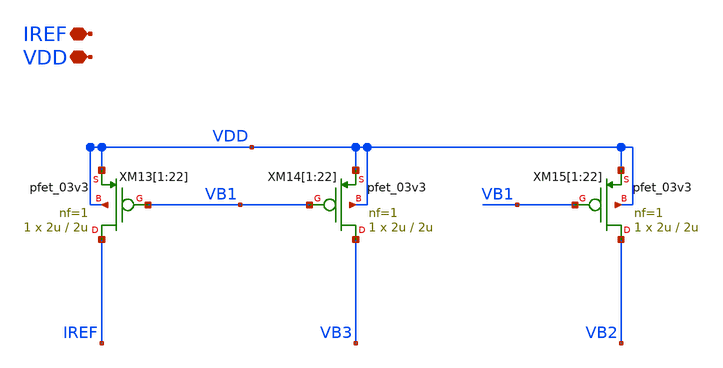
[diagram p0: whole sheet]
** sch_path: TIA_Filter/Folded/FC_bias_pfets.sch
**.subckt FC_bias_pfets IREF VDD
*.iopin IREF
*.iopin VDD
XM13[1] IREF VB1 VDD VDD pfet_03v3 L=2u W=2u nf=1 ad='int((nf+1)/2) * W/nf * 0.18u' as='int((nf+2)/2) * W/nf * 0.18u'
+ pd='2*int((nf+1)/2) * (W/nf + 0.18u)' ps='2*int((nf+2)/2) * (W/nf + 0.18u)' nrd='0.18u / W' nrs='0.18u / W'
+ sa=0 sb=0 sd=0 m=1
XM13[2] IREF VB1 VDD VDD pfet_03v3 L=2u W=2u nf=1 ad='int((nf+1)/2) * W/nf * 0.18u' as='int((nf+2)/2) * W/nf * 0.18u'
+ pd='2*int((nf+1)/2) * (W/nf + 0.18u)' ps='2*int((nf+2)/2) * (W/nf + 0.18u)' nrd='0.18u / W' nrs='0.18u / W'
+ sa=0 sb=0 sd=0 m=1
XM13[3] IREF VB1 VDD VDD pfet_03v3 L=2u W=2u nf=1 ad='int((nf+1)/2) * W/nf * 0.18u' as='int((nf+2)/2) * W/nf * 0.18u'
+ pd='2*int((nf+1)/2) * (W/nf + 0.18u)' ps='2*int((nf+2)/2) * (W/nf + 0.18u)' nrd='0.18u / W' nrs='0.18u / W'
+ sa=0 sb=0 sd=0 m=1
XM13[4] IREF VB1 VDD VDD pfet_03v3 L=2u W=2u nf=1 ad='int((nf+1)/2) * W/nf * 0.18u' as='int((nf+2)/2) * W/nf * 0.18u'
+ pd='2*int((nf+1)/2) * (W/nf + 0.18u)' ps='2*int((nf+2)/2) * (W/nf + 0.18u)' nrd='0.18u / W' nrs='0.18u / W'
+ sa=0 sb=0 sd=0 m=1
XM13[5] IREF VB1 VDD VDD pfet_03v3 L=2u W=2u nf=1 ad='int((nf+1)/2) * W/nf * 0.18u' as='int((nf+2)/2) * W/nf * 0.18u'
+ pd='2*int((nf+1)/2) * (W/nf + 0.18u)' ps='2*int((nf+2)/2) * (W/nf + 0.18u)' nrd='0.18u / W' nrs='0.18u / W'
+ sa=0 sb=0 sd=0 m=1
XM13[6] IREF VB1 VDD VDD pfet_03v3 L=2u W=2u nf=1 ad='int((nf+1)/2) * W/nf * 0.18u' as='int((nf+2)/2) * W/nf * 0.18u'
+ pd='2*int((nf+1)/2) * (W/nf + 0.18u)' ps='2*int((nf+2)/2) * (W/nf + 0.18u)' nrd='0.18u / W' nrs='0.18u / W'
+ sa=0 sb=0 sd=0 m=1
XM13[7] IREF VB1 VDD VDD pfet_03v3 L=2u W=2u nf=1 ad='int((nf+1)/2) * W/nf * 0.18u' as='int((nf+2)/2) * W/nf * 0.18u'
+ pd='2*int((nf+1)/2) * (W/nf + 0.18u)' ps='2*int((nf+2)/2) * (W/nf + 0.18u)' nrd='0.18u / W' nrs='0.18u / W'
+ sa=0 sb=0 sd=0 m=1
XM13[8] IREF VB1 VDD VDD pfet_03v3 L=2u W=2u nf=1 ad='int((nf+1)/2) * W/nf * 0.18u' as='int((nf+2)/2) * W/nf * 0.18u'
+ pd='2*int((nf+1)/2) * (W/nf + 0.18u)' ps='2*int((nf+2)/2) * (W/nf + 0.18u)' nrd='0.18u / W' nrs='0.18u / W'
+ sa=0 sb=0 sd=0 m=1
XM13[9] IREF VB1 VDD VDD pfet_03v3 L=2u W=2u nf=1 ad='int((nf+1)/2) * W/nf * 0.18u' as='int((nf+2)/2) * W/nf * 0.18u'
+ pd='2*int((nf+1)/2) * (W/nf + 0.18u)' ps='2*int((nf+2)/2) * (W/nf + 0.18u)' nrd='0.18u / W' nrs='0.18u / W'
+ sa=0 sb=0 sd=0 m=1
XM13[10] IREF VB1 VDD VDD pfet_03v3 L=2u W=2u nf=1 ad='int((nf+1)/2) * W/nf * 0.18u' as='int((nf+2)/2) * W/nf * 0.18u'
+ pd='2*int((nf+1)/2) * (W/nf + 0.18u)' ps='2*int((nf+2)/2) * (W/nf + 0.18u)' nrd='0.18u / W' nrs='0.18u / W'
+ sa=0 sb=0 sd=0 m=1
XM13[11] IREF VB1 VDD VDD pfet_03v3 L=2u W=2u nf=1 ad='int((nf+1)/2) * W/nf * 0.18u' as='int((nf+2)/2) * W/nf * 0.18u'
+ pd='2*int((nf+1)/2) * (W/nf + 0.18u)' ps='2*int((nf+2)/2) * (W/nf + 0.18u)' nrd='0.18u / W' nrs='0.18u / W'
+ sa=0 sb=0 sd=0 m=1
XM13[12] IREF VB1 VDD VDD pfet_03v3 L=2u W=2u nf=1 ad='int((nf+1)/2) * W/nf * 0.18u' as='int((nf+2)/2) * W/nf * 0.18u'
+ pd='2*int((nf+1)/2) * (W/nf + 0.18u)' ps='2*int((nf+2)/2) * (W/nf + 0.18u)' nrd='0.18u / W' nrs='0.18u / W'
+ sa=0 sb=0 sd=0 m=1
XM13[13] IREF VB1 VDD VDD pfet_03v3 L=2u W=2u nf=1 ad='int((nf+1)/2) * W/nf * 0.18u' as='int((nf+2)/2) * W/nf * 0.18u'
+ pd='2*int((nf+1)/2) * (W/nf + 0.18u)' ps='2*int((nf+2)/2) * (W/nf + 0.18u)' nrd='0.18u / W' nrs='0.18u / W'
+ sa=0 sb=0 sd=0 m=1
XM13[14] IREF VB1 VDD VDD pfet_03v3 L=2u W=2u nf=1 ad='int((nf+1)/2) * W/nf * 0.18u' as='int((nf+2)/2) * W/nf * 0.18u'
+ pd='2*int((nf+1)/2) * (W/nf + 0.18u)' ps='2*int((nf+2)/2) * (W/nf + 0.18u)' nrd='0.18u / W' nrs='0.18u / W'
+ sa=0 sb=0 sd=0 m=1
XM13[15] IREF VB1 VDD VDD pfet_03v3 L=2u W=2u nf=1 ad='int((nf+1)/2) * W/nf * 0.18u' as='int((nf+2)/2) * W/nf * 0.18u'
+ pd='2*int((nf+1)/2) * (W/nf + 0.18u)' ps='2*int((nf+2)/2) * (W/nf + 0.18u)' nrd='0.18u / W' nrs='0.18u / W'
+ sa=0 sb=0 sd=0 m=1
XM13[16] IREF VB1 VDD VDD pfet_03v3 L=2u W=2u nf=1 ad='int((nf+1)/2) * W/nf * 0.18u' as='int((nf+2)/2) * W/nf * 0.18u'
+ pd='2*int((nf+1)/2) * (W/nf + 0.18u)' ps='2*int((nf+2)/2) * (W/nf + 0.18u)' nrd='0.18u / W' nrs='0.18u / W'
+ sa=0 sb=0 sd=0 m=1
XM13[17] IREF VB1 VDD VDD pfet_03v3 L=2u W=2u nf=1 ad='int((nf+1)/2) * W/nf * 0.18u' as='int((nf+2)/2) * W/nf * 0.18u'
+ pd='2*int((nf+1)/2) * (W/nf + 0.18u)' ps='2*int((nf+2)/2) * (W/nf + 0.18u)' nrd='0.18u / W' nrs='0.18u / W'
+ sa=0 sb=0 sd=0 m=1
XM13[18] IREF VB1 VDD VDD pfet_03v3 L=2u W=2u nf=1 ad='int((nf+1)/2) * W/nf * 0.18u' as='int((nf+2)/2) * W/nf * 0.18u'
+ pd='2*int((nf+1)/2) * (W/nf + 0.18u)' ps='2*int((nf+2)/2) * (W/nf + 0.18u)' nrd='0.18u / W' nrs='0.18u / W'
+ sa=0 sb=0 sd=0 m=1
XM13[19] IREF VB1 VDD VDD pfet_03v3 L=2u W=2u nf=1 ad='int((nf+1)/2) * W/nf * 0.18u' as='int((nf+2)/2) * W/nf * 0.18u'
+ pd='2*int((nf+1)/2) * (W/nf + 0.18u)' ps='2*int((nf+2)/2) * (W/nf + 0.18u)' nrd='0.18u / W' nrs='0.18u / W'
+ sa=0 sb=0 sd=0 m=1
XM13[20] IREF VB1 VDD VDD pfet_03v3 L=2u W=2u nf=1 ad='int((nf+1)/2) * W/nf * 0.18u' as='int((nf+2)/2) * W/nf * 0.18u'
+ pd='2*int((nf+1)/2) * (W/nf + 0.18u)' ps='2*int((nf+2)/2) * (W/nf + 0.18u)' nrd='0.18u / W' nrs='0.18u / W'
+ sa=0 sb=0 sd=0 m=1
XM13[21] IREF VB1 VDD VDD pfet_03v3 L=2u W=2u nf=1 ad='int((nf+1)/2) * W/nf * 0.18u' as='int((nf+2)/2) * W/nf * 0.18u'
+ pd='2*int((nf+1)/2) * (W/nf + 0.18u)' ps='2*int((nf+2)/2) * (W/nf + 0.18u)' nrd='0.18u / W' nrs='0.18u / W'
+ sa=0 sb=0 sd=0 m=1
XM13[22] IREF VB1 VDD VDD pfet_03v3 L=2u W=2u nf=1 ad='int((nf+1)/2) * W/nf * 0.18u' as='int((nf+2)/2) * W/nf * 0.18u'
+ pd='2*int((nf+1)/2) * (W/nf + 0.18u)' ps='2*int((nf+2)/2) * (W/nf + 0.18u)' nrd='0.18u / W' nrs='0.18u / W'
+ sa=0 sb=0 sd=0 m=1
XM14[1] VB3 VB1 VDD VDD pfet_03v3 L=2u W=2u nf=1 ad='int((nf+1)/2) * W/nf * 0.18u' as='int((nf+2)/2) * W/nf * 0.18u'
+ pd='2*int((nf+1)/2) * (W/nf + 0.18u)' ps='2*int((nf+2)/2) * (W/nf + 0.18u)' nrd='0.18u / W' nrs='0.18u / W'
+ sa=0 sb=0 sd=0 m=1
XM14[2] VB3 VB1 VDD VDD pfet_03v3 L=2u W=2u nf=1 ad='int((nf+1)/2) * W/nf * 0.18u' as='int((nf+2)/2) * W/nf * 0.18u'
+ pd='2*int((nf+1)/2) * (W/nf + 0.18u)' ps='2*int((nf+2)/2) * (W/nf + 0.18u)' nrd='0.18u / W' nrs='0.18u / W'
+ sa=0 sb=0 sd=0 m=1
XM14[3] VB3 VB1 VDD VDD pfet_03v3 L=2u W=2u nf=1 ad='int((nf+1)/2) * W/nf * 0.18u' as='int((nf+2)/2) * W/nf * 0.18u'
+ pd='2*int((nf+1)/2) * (W/nf + 0.18u)' ps='2*int((nf+2)/2) * (W/nf + 0.18u)' nrd='0.18u / W' nrs='0.18u / W'
+ sa=0 sb=0 sd=0 m=1
XM14[4] VB3 VB1 VDD VDD pfet_03v3 L=2u W=2u nf=1 ad='int((nf+1)/2) * W/nf * 0.18u' as='int((nf+2)/2) * W/nf * 0.18u'
+ pd='2*int((nf+1)/2) * (W/nf + 0.18u)' ps='2*int((nf+2)/2) * (W/nf + 0.18u)' nrd='0.18u / W' nrs='0.18u / W'
+ sa=0 sb=0 sd=0 m=1
XM14[5] VB3 VB1 VDD VDD pfet_03v3 L=2u W=2u nf=1 ad='int((nf+1)/2) * W/nf * 0.18u' as='int((nf+2)/2) * W/nf * 0.18u'
+ pd='2*int((nf+1)/2) * (W/nf + 0.18u)' ps='2*int((nf+2)/2) * (W/nf + 0.18u)' nrd='0.18u / W' nrs='0.18u / W'
+ sa=0 sb=0 sd=0 m=1
XM14[6] VB3 VB1 VDD VDD pfet_03v3 L=2u W=2u nf=1 ad='int((nf+1)/2) * W/nf * 0.18u' as='int((nf+2)/2) * W/nf * 0.18u'
+ pd='2*int((nf+1)/2) * (W/nf + 0.18u)' ps='2*int((nf+2)/2) * (W/nf + 0.18u)' nrd='0.18u / W' nrs='0.18u / W'
+ sa=0 sb=0 sd=0 m=1
XM14[7] VB3 VB1 VDD VDD pfet_03v3 L=2u W=2u nf=1 ad='int((nf+1)/2) * W/nf * 0.18u' as='int((nf+2)/2) * W/nf * 0.18u'
+ pd='2*int((nf+1)/2) * (W/nf + 0.18u)' ps='2*int((nf+2)/2) * (W/nf + 0.18u)' nrd='0.18u / W' nrs='0.18u / W'
+ sa=0 sb=0 sd=0 m=1
XM14[8] VB3 VB1 VDD VDD pfet_03v3 L=2u W=2u nf=1 ad='int((nf+1)/2) * W/nf * 0.18u' as='int((nf+2)/2) * W/nf * 0.18u'
+ pd='2*int((nf+1)/2) * (W/nf + 0.18u)' ps='2*int((nf+2)/2) * (W/nf + 0.18u)' nrd='0.18u / W' nrs='0.18u / W'
+ sa=0 sb=0 sd=0 m=1
XM14[9] VB3 VB1 VDD VDD pfet_03v3 L=2u W=2u nf=1 ad='int((nf+1)/2) * W/nf * 0.18u' as='int((nf+2)/2) * W/nf * 0.18u'
+ pd='2*int((nf+1)/2) * (W/nf + 0.18u)' ps='2*int((nf+2)/2) * (W/nf + 0.18u)' nrd='0.18u / W' nrs='0.18u / W'
+ sa=0 sb=0 sd=0 m=1
XM14[10] VB3 VB1 VDD VDD pfet_03v3 L=2u W=2u nf=1 ad='int((nf+1)/2) * W/nf * 0.18u' as='int((nf+2)/2) * W/nf * 0.18u'
+ pd='2*int((nf+1)/2) * (W/nf + 0.18u)' ps='2*int((nf+2)/2) * (W/nf + 0.18u)' nrd='0.18u / W' nrs='0.18u / W'
+ sa=0 sb=0 sd=0 m=1
XM14[11] VB3 VB1 VDD VDD pfet_03v3 L=2u W=2u nf=1 ad='int((nf+1)/2) * W/nf * 0.18u' as='int((nf+2)/2) * W/nf * 0.18u'
+ pd='2*int((nf+1)/2) * (W/nf + 0.18u)' ps='2*int((nf+2)/2) * (W/nf + 0.18u)' nrd='0.18u / W' nrs='0.18u / W'
+ sa=0 sb=0 sd=0 m=1
XM14[12] VB3 VB1 VDD VDD pfet_03v3 L=2u W=2u nf=1 ad='int((nf+1)/2) * W/nf * 0.18u' as='int((nf+2)/2) * W/nf * 0.18u'
+ pd='2*int((nf+1)/2) * (W/nf + 0.18u)' ps='2*int((nf+2)/2) * (W/nf + 0.18u)' nrd='0.18u / W' nrs='0.18u / W'
+ sa=0 sb=0 sd=0 m=1
XM14[13] VB3 VB1 VDD VDD pfet_03v3 L=2u W=2u nf=1 ad='int((nf+1)/2) * W/nf * 0.18u' as='int((nf+2)/2) * W/nf * 0.18u'
+ pd='2*int((nf+1)/2) * (W/nf + 0.18u)' ps='2*int((nf+2)/2) * (W/nf + 0.18u)' nrd='0.18u / W' nrs='0.18u / W'
+ sa=0 sb=0 sd=0 m=1
XM14[14] VB3 VB1 VDD VDD pfet_03v3 L=2u W=2u nf=1 ad='int((nf+1)/2) * W/nf * 0.18u' as='int((nf+2)/2) * W/nf * 0.18u'
+ pd='2*int((nf+1)/2) * (W/nf + 0.18u)' ps='2*int((nf+2)/2) * (W/nf + 0.18u)' nrd='0.18u / W' nrs='0.18u / W'
+ sa=0 sb=0 sd=0 m=1
XM14[15] VB3 VB1 VDD VDD pfet_03v3 L=2u W=2u nf=1 ad='int((nf+1)/2) * W/nf * 0.18u' as='int((nf+2)/2) * W/nf * 0.18u'
+ pd='2*int((nf+1)/2) * (W/nf + 0.18u)' ps='2*int((nf+2)/2) * (W/nf + 0.18u)' nrd='0.18u / W' nrs='0.18u / W'
+ sa=0 sb=0 sd=0 m=1
XM14[16] VB3 VB1 VDD VDD pfet_03v3 L=2u W=2u nf=1 ad='int((nf+1)/2) * W/nf * 0.18u' as='int((nf+2)/2) * W/nf * 0.18u'
+ pd='2*int((nf+1)/2) * (W/nf + 0.18u)' ps='2*int((nf+2)/2) * (W/nf + 0.18u)' nrd='0.18u / W' nrs='0.18u / W'
+ sa=0 sb=0 sd=0 m=1
XM14[17] VB3 VB1 VDD VDD pfet_03v3 L=2u W=2u nf=1 ad='int((nf+1)/2) * W/nf * 0.18u' as='int((nf+2)/2) * W/nf * 0.18u'
+ pd='2*int((nf+1)/2) * (W/nf + 0.18u)' ps='2*int((nf+2)/2) * (W/nf + 0.18u)' nrd='0.18u / W' nrs='0.18u / W'
+ sa=0 sb=0 sd=0 m=1
XM14[18] VB3 VB1 VDD VDD pfet_03v3 L=2u W=2u nf=1 ad='int((nf+1)/2) * W/nf * 0.18u' as='int((nf+2)/2) * W/nf * 0.18u'
+ pd='2*int((nf+1)/2) * (W/nf + 0.18u)' ps='2*int((nf+2)/2) * (W/nf + 0.18u)' nrd='0.18u / W' nrs='0.18u / W'
+ sa=0 sb=0 sd=0 m=1
XM14[19] VB3 VB1 VDD VDD pfet_03v3 L=2u W=2u nf=1 ad='int((nf+1)/2) * W/nf * 0.18u' as='int((nf+2)/2) * W/nf * 0.18u'
+ pd='2*int((nf+1)/2) * (W/nf + 0.18u)' ps='2*int((nf+2)/2) * (W/nf + 0.18u)' nrd='0.18u / W' nrs='0.18u / W'
+ sa=0 sb=0 sd=0 m=1
XM14[20] VB3 VB1 VDD VDD pfet_03v3 L=2u W=2u nf=1 ad='int((nf+1)/2) * W/nf * 0.18u' as='int((nf+2)/2) * W/nf * 0.18u'
+ pd='2*int((nf+1)/2) * (W/nf + 0.18u)' ps='2*int((nf+2)/2) * (W/nf + 0.18u)' nrd='0.18u / W' nrs='0.18u / W'
+ sa=0 sb=0 sd=0 m=1
XM14[21] VB3 VB1 VDD VDD pfet_03v3 L=2u W=2u nf=1 ad='int((nf+1)/2) * W/nf * 0.18u' as='int((nf+2)/2) * W/nf * 0.18u'
+ pd='2*int((nf+1)/2) * (W/nf + 0.18u)' ps='2*int((nf+2)/2) * (W/nf + 0.18u)' nrd='0.18u / W' nrs='0.18u / W'
+ sa=0 sb=0 sd=0 m=1
XM14[22] VB3 VB1 VDD VDD pfet_03v3 L=2u W=2u nf=1 ad='int((nf+1)/2) * W/nf * 0.18u' as='int((nf+2)/2) * W/nf * 0.18u'
+ pd='2*int((nf+1)/2) * (W/nf + 0.18u)' ps='2*int((nf+2)/2) * (W/nf + 0.18u)' nrd='0.18u / W' nrs='0.18u / W'
+ sa=0 sb=0 sd=0 m=1
XM15[1] VB2 VB1 VDD VDD pfet_03v3 L=2u W=2u nf=1 ad='int((nf+1)/2) * W/nf * 0.18u' as='int((nf+2)/2) * W/nf * 0.18u'
+ pd='2*int((nf+1)/2) * (W/nf + 0.18u)' ps='2*int((nf+2)/2) * (W/nf + 0.18u)' nrd='0.18u / W' nrs='0.18u / W'
+ sa=0 sb=0 sd=0 m=1
XM15[2] VB2 VB1 VDD VDD pfet_03v3 L=2u W=2u nf=1 ad='int((nf+1)/2) * W/nf * 0.18u' as='int((nf+2)/2) * W/nf * 0.18u'
+ pd='2*int((nf+1)/2) * (W/nf + 0.18u)' ps='2*int((nf+2)/2) * (W/nf + 0.18u)' nrd='0.18u / W' nrs='0.18u / W'
+ sa=0 sb=0 sd=0 m=1
XM15[3] VB2 VB1 VDD VDD pfet_03v3 L=2u W=2u nf=1 ad='int((nf+1)/2) * W/nf * 0.18u' as='int((nf+2)/2) * W/nf * 0.18u'
+ pd='2*int((nf+1)/2) * (W/nf + 0.18u)' ps='2*int((nf+2)/2) * (W/nf + 0.18u)' nrd='0.18u / W' nrs='0.18u / W'
+ sa=0 sb=0 sd=0 m=1
XM15[4] VB2 VB1 VDD VDD pfet_03v3 L=2u W=2u nf=1 ad='int((nf+1)/2) * W/nf * 0.18u' as='int((nf+2)/2) * W/nf * 0.18u'
+ pd='2*int((nf+1)/2) * (W/nf + 0.18u)' ps='2*int((nf+2)/2) * (W/nf + 0.18u)' nrd='0.18u / W' nrs='0.18u / W'
+ sa=0 sb=0 sd=0 m=1
XM15[5] VB2 VB1 VDD VDD pfet_03v3 L=2u W=2u nf=1 ad='int((nf+1)/2) * W/nf * 0.18u' as='int((nf+2)/2) * W/nf * 0.18u'
+ pd='2*int((nf+1)/2) * (W/nf + 0.18u)' ps='2*int((nf+2)/2) * (W/nf + 0.18u)' nrd='0.18u / W' nrs='0.18u / W'
+ sa=0 sb=0 sd=0 m=1
XM15[6] VB2 VB1 VDD VDD pfet_03v3 L=2u W=2u nf=1 ad='int((nf+1)/2) * W/nf * 0.18u' as='int((nf+2)/2) * W/nf * 0.18u'
+ pd='2*int((nf+1)/2) * (W/nf + 0.18u)' ps='2*int((nf+2)/2) * (W/nf + 0.18u)' nrd='0.18u / W' nrs='0.18u / W'
+ sa=0 sb=0 sd=0 m=1
XM15[7] VB2 VB1 VDD VDD pfet_03v3 L=2u W=2u nf=1 ad='int((nf+1)/2) * W/nf * 0.18u' as='int((nf+2)/2) * W/nf * 0.18u'
+ pd='2*int((nf+1)/2) * (W/nf + 0.18u)' ps='2*int((nf+2)/2) * (W/nf + 0.18u)' nrd='0.18u / W' nrs='0.18u / W'
+ sa=0 sb=0 sd=0 m=1
XM15[8] VB2 VB1 VDD VDD pfet_03v3 L=2u W=2u nf=1 ad='int((nf+1)/2) * W/nf * 0.18u' as='int((nf+2)/2) * W/nf * 0.18u'
+ pd='2*int((nf+1)/2) * (W/nf + 0.18u)' ps='2*int((nf+2)/2) * (W/nf + 0.18u)' nrd='0.18u / W' nrs='0.18u / W'
+ sa=0 sb=0 sd=0 m=1
XM15[9] VB2 VB1 VDD VDD pfet_03v3 L=2u W=2u nf=1 ad='int((nf+1)/2) * W/nf * 0.18u' as='int((nf+2)/2) * W/nf * 0.18u'
+ pd='2*int((nf+1)/2) * (W/nf + 0.18u)' ps='2*int((nf+2)/2) * (W/nf + 0.18u)' nrd='0.18u / W' nrs='0.18u / W'
+ sa=0 sb=0 sd=0 m=1
XM15[10] VB2 VB1 VDD VDD pfet_03v3 L=2u W=2u nf=1 ad='int((nf+1)/2) * W/nf * 0.18u' as='int((nf+2)/2) * W/nf * 0.18u'
+ pd='2*int((nf+1)/2) * (W/nf + 0.18u)' ps='2*int((nf+2)/2) * (W/nf + 0.18u)' nrd='0.18u / W' nrs='0.18u / W'
+ sa=0 sb=0 sd=0 m=1
XM15[11] VB2 VB1 VDD VDD pfet_03v3 L=2u W=2u nf=1 ad='int((nf+1)/2) * W/nf * 0.18u' as='int((nf+2)/2) * W/nf * 0.18u'
+ pd='2*int((nf+1)/2) * (W/nf + 0.18u)' ps='2*int((nf+2)/2) * (W/nf + 0.18u)' nrd='0.18u / W' nrs='0.18u / W'
+ sa=0 sb=0 sd=0 m=1
XM15[12] VB2 VB1 VDD VDD pfet_03v3 L=2u W=2u nf=1 ad='int((nf+1)/2) * W/nf * 0.18u' as='int((nf+2)/2) * W/nf * 0.18u'
+ pd='2*int((nf+1)/2) * (W/nf + 0.18u)' ps='2*int((nf+2)/2) * (W/nf + 0.18u)' nrd='0.18u / W' nrs='0.18u / W'
+ sa=0 sb=0 sd=0 m=1
XM15[13] VB2 VB1 VDD VDD pfet_03v3 L=2u W=2u nf=1 ad='int((nf+1)/2) * W/nf * 0.18u' as='int((nf+2)/2) * W/nf * 0.18u'
+ pd='2*int((nf+1)/2) * (W/nf + 0.18u)' ps='2*int((nf+2)/2) * (W/nf + 0.18u)' nrd='0.18u / W' nrs='0.18u / W'
+ sa=0 sb=0 sd=0 m=1
XM15[14] VB2 VB1 VDD VDD pfet_03v3 L=2u W=2u nf=1 ad='int((nf+1)/2) * W/nf * 0.18u' as='int((nf+2)/2) * W/nf * 0.18u'
+ pd='2*int((nf+1)/2) * (W/nf + 0.18u)' ps='2*int((nf+2)/2) * (W/nf + 0.18u)' nrd='0.18u / W' nrs='0.18u / W'
+ sa=0 sb=0 sd=0 m=1
XM15[15] VB2 VB1 VDD VDD pfet_03v3 L=2u W=2u nf=1 ad='int((nf+1)/2) * W/nf * 0.18u' as='int((nf+2)/2) * W/nf * 0.18u'
+ pd='2*int((nf+1)/2) * (W/nf + 0.18u)' ps='2*int((nf+2)/2) * (W/nf + 0.18u)' nrd='0.18u / W' nrs='0.18u / W'
+ sa=0 sb=0 sd=0 m=1
XM15[16] VB2 VB1 VDD VDD pfet_03v3 L=2u W=2u nf=1 ad='int((nf+1)/2) * W/nf * 0.18u' as='int((nf+2)/2) * W/nf * 0.18u'
+ pd='2*int((nf+1)/2) * (W/nf + 0.18u)' ps='2*int((nf+2)/2) * (W/nf + 0.18u)' nrd='0.18u / W' nrs='0.18u / W'
+ sa=0 sb=0 sd=0 m=1
XM15[17] VB2 VB1 VDD VDD pfet_03v3 L=2u W=2u nf=1 ad='int((nf+1)/2) * W/nf * 0.18u' as='int((nf+2)/2) * W/nf * 0.18u'
+ pd='2*int((nf+1)/2) * (W/nf + 0.18u)' ps='2*int((nf+2)/2) * (W/nf + 0.18u)' nrd='0.18u / W' nrs='0.18u / W'
+ sa=0 sb=0 sd=0 m=1
XM15[18] VB2 VB1 VDD VDD pfet_03v3 L=2u W=2u nf=1 ad='int((nf+1)/2) * W/nf * 0.18u' as='int((nf+2)/2) * W/nf * 0.18u'
+ pd='2*int((nf+1)/2) * (W/nf + 0.18u)' ps='2*int((nf+2)/2) * (W/nf + 0.18u)' nrd='0.18u / W' nrs='0.18u / W'
+ sa=0 sb=0 sd=0 m=1
XM15[19] VB2 VB1 VDD VDD pfet_03v3 L=2u W=2u nf=1 ad='int((nf+1)/2) * W/nf * 0.18u' as='int((nf+2)/2) * W/nf * 0.18u'
+ pd='2*int((nf+1)/2) * (W/nf + 0.18u)' ps='2*int((nf+2)/2) * (W/nf + 0.18u)' nrd='0.18u / W' nrs='0.18u / W'
+ sa=0 sb=0 sd=0 m=1
XM15[20] VB2 VB1 VDD VDD pfet_03v3 L=2u W=2u nf=1 ad='int((nf+1)/2) * W/nf * 0.18u' as='int((nf+2)/2) * W/nf * 0.18u'
+ pd='2*int((nf+1)/2) * (W/nf + 0.18u)' ps='2*int((nf+2)/2) * (W/nf + 0.18u)' nrd='0.18u / W' nrs='0.18u / W'
+ sa=0 sb=0 sd=0 m=1
XM15[21] VB2 VB1 VDD VDD pfet_03v3 L=2u W=2u nf=1 ad='int((nf+1)/2) * W/nf * 0.18u' as='int((nf+2)/2) * W/nf * 0.18u'
+ pd='2*int((nf+1)/2) * (W/nf + 0.18u)' ps='2*int((nf+2)/2) * (W/nf + 0.18u)' nrd='0.18u / W' nrs='0.18u / W'
+ sa=0 sb=0 sd=0 m=1
XM15[22] VB2 VB1 VDD VDD pfet_03v3 L=2u W=2u nf=1 ad='int((nf+1)/2) * W/nf * 0.18u' as='int((nf+2)/2) * W/nf * 0.18u'
+ pd='2*int((nf+1)/2) * (W/nf + 0.18u)' ps='2*int((nf+2)/2) * (W/nf + 0.18u)' nrd='0.18u / W' nrs='0.18u / W'
+ sa=0 sb=0 sd=0 m=1
**.ends
.end
